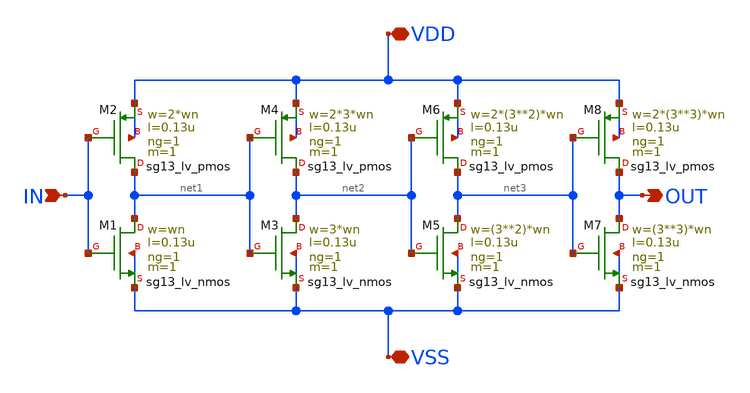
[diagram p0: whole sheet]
** sch_path: SSDOR_1V_v1/components/buffer4/buffer4.sch
**.subckt buffer4 VDD VSS IN OUT
*.iopin VDD
*.iopin VSS
*.ipin IN
*.opin OUT
XM1 net1 IN VSS VSS sg13_lv_nmos w=wn l=0.13u ng=1 m=1 mm_ok=1
XM2 net1 IN VDD VDD sg13_lv_pmos w=2*wn l=0.13u ng=1 m=1 mm_ok=1
XM3 net2 net1 VSS VSS sg13_lv_nmos w=3*wn l=0.13u ng=1 m=1 mm_ok=1
XM4 net2 net1 VDD VDD sg13_lv_pmos w=2*3*wn l=0.13u ng=1 m=1 mm_ok=1
XM5 net3 net2 VSS VSS sg13_lv_nmos w=(3**2)*wn l=0.13u ng=1 m=1 mm_ok=1
XM6 net3 net2 VDD VDD sg13_lv_pmos w=2*(3**2)*wn l=0.13u ng=1 m=1 mm_ok=1
XM7 OUT net3 VSS VSS sg13_lv_nmos w=(3**3)*wn l=0.13u ng=1 m=1 mm_ok=1
XM8 OUT net3 VDD VDD sg13_lv_pmos w=2*(3**3)*wn l=0.13u ng=1 m=1 mm_ok=1
**.ends
.end
